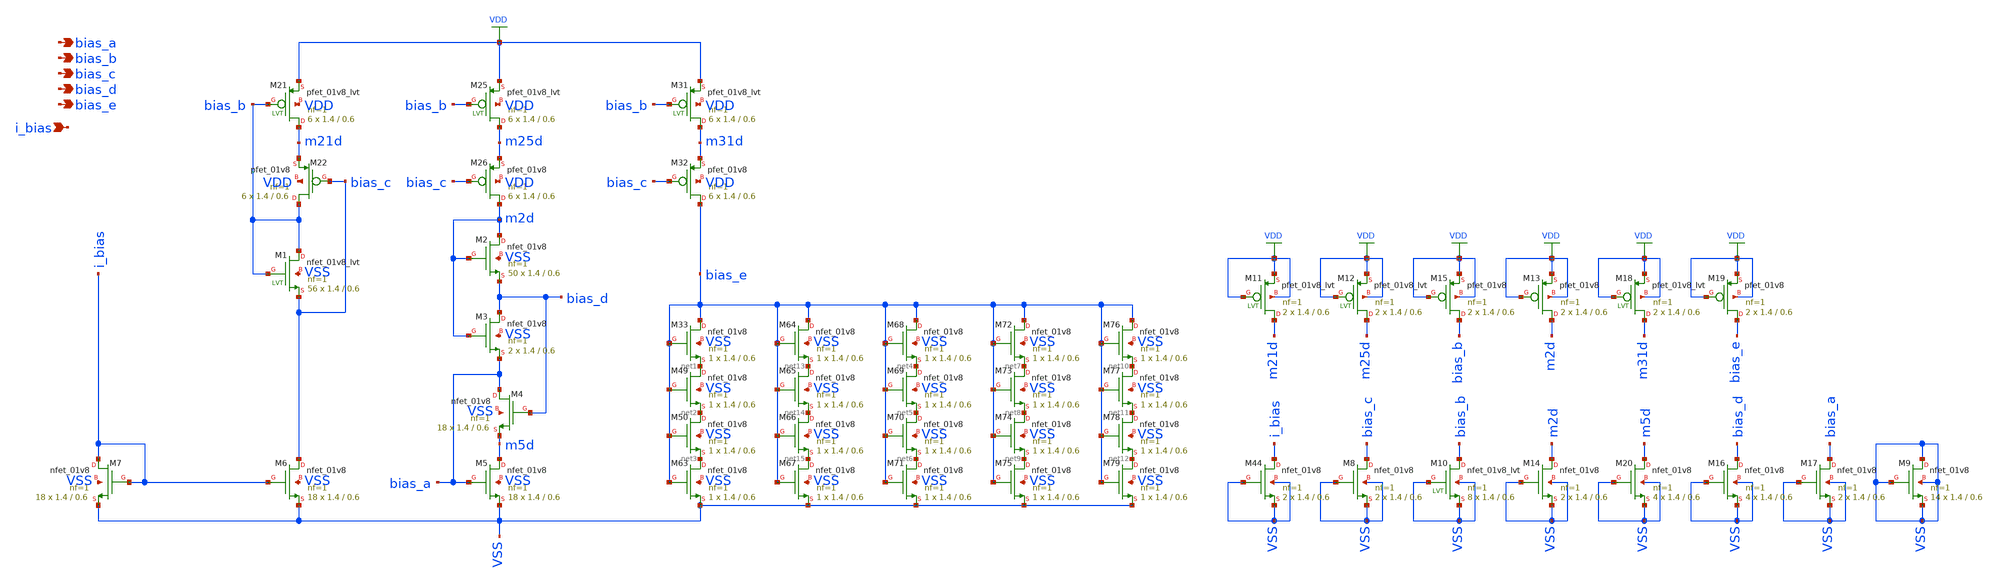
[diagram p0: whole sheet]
** sch_path: design/analog_modulator/schematic/folded_cascode_3_bias.sch
**.subckt folded_cascode_3_bias bias_a bias_b bias_c bias_d bias_e i_bias
*.opin bias_a
*.opin bias_b
*.opin bias_c
*.opin bias_d
*.opin bias_e
*.ipin i_bias
XM22 bias_b bias_c m21d VDD sky130_fd_pr__pfet_01v8 L=0.6 W=1.4 nf=1 ad='int((nf+1)/2) * W/nf * 0.29'
+ as='int((nf+2)/2) * W/nf * 0.29' pd='2*int((nf+1)/2) * (W/nf + 0.29)' ps='2*int((nf+2)/2) * (W/nf + 0.29)'
+ nrd='0.29 / W' nrs='0.29 / W' sa=0 sb=0 sd=0 mult=6 m=6
XM26 m2d bias_c m25d VDD sky130_fd_pr__pfet_01v8 L=0.6 W=1.4 nf=1 ad='int((nf+1)/2) * W/nf * 0.29' as='int((nf+2)/2) * W/nf * 0.29'
+ pd='2*int((nf+1)/2) * (W/nf + 0.29)' ps='2*int((nf+2)/2) * (W/nf + 0.29)' nrd='0.29 / W' nrs='0.29 / W'
+ sa=0 sb=0 sd=0 mult=6 m=6
XM32 bias_e bias_c m31d VDD sky130_fd_pr__pfet_01v8 L=0.6 W=1.4 nf=1 ad='int((nf+1)/2) * W/nf * 0.29'
+ as='int((nf+2)/2) * W/nf * 0.29' pd='2*int((nf+1)/2) * (W/nf + 0.29)' ps='2*int((nf+2)/2) * (W/nf + 0.29)'
+ nrd='0.29 / W' nrs='0.29 / W' sa=0 sb=0 sd=0 mult=6 m=6
XM21 m21d bias_b VDD VDD sky130_fd_pr__pfet_01v8_lvt L=0.6 W=1.4 nf=1 ad='int((nf+1)/2) * W/nf * 0.29'
+ as='int((nf+2)/2) * W/nf * 0.29' pd='2*int((nf+1)/2) * (W/nf + 0.29)' ps='2*int((nf+2)/2) * (W/nf + 0.29)'
+ nrd='0.29 / W' nrs='0.29 / W' sa=0 sb=0 sd=0 mult=6 m=6
XM25 m25d bias_b VDD VDD sky130_fd_pr__pfet_01v8_lvt L=0.6 W=1.4 nf=1 ad='int((nf+1)/2) * W/nf * 0.29'
+ as='int((nf+2)/2) * W/nf * 0.29' pd='2*int((nf+1)/2) * (W/nf + 0.29)' ps='2*int((nf+2)/2) * (W/nf + 0.29)'
+ nrd='0.29 / W' nrs='0.29 / W' sa=0 sb=0 sd=0 mult=6 m=6
XM31 m31d bias_b VDD VDD sky130_fd_pr__pfet_01v8_lvt L=0.6 W=1.4 nf=1 ad='int((nf+1)/2) * W/nf * 0.29'
+ as='int((nf+2)/2) * W/nf * 0.29' pd='2*int((nf+1)/2) * (W/nf + 0.29)' ps='2*int((nf+2)/2) * (W/nf + 0.29)'
+ nrd='0.29 / W' nrs='0.29 / W' sa=0 sb=0 sd=0 mult=6 m=6
XM1 bias_b bias_b bias_c VSS sky130_fd_pr__nfet_01v8_lvt L=0.6 W=1.4 nf=1 ad='int((nf+1)/2) * W/nf * 0.29'
+ as='int((nf+2)/2) * W/nf * 0.29' pd='2*int((nf+1)/2) * (W/nf + 0.29)' ps='2*int((nf+2)/2) * (W/nf + 0.29)'
+ nrd='0.29 / W' nrs='0.29 / W' sa=0 sb=0 sd=0 mult=56 m=56
XM2 m2d m2d bias_d VSS sky130_fd_pr__nfet_01v8 L=0.6 W=1.4 nf=1 ad='int((nf+1)/2) * W/nf * 0.29' as='int((nf+2)/2) * W/nf * 0.29'
+ pd='2*int((nf+1)/2) * (W/nf + 0.29)' ps='2*int((nf+2)/2) * (W/nf + 0.29)' nrd='0.29 / W' nrs='0.29 / W'
+ sa=0 sb=0 sd=0 mult=50 m=50
XM3 bias_d m2d bias_a VSS sky130_fd_pr__nfet_01v8 L=0.6 W=1.4 nf=1 ad='int((nf+1)/2) * W/nf * 0.29' as='int((nf+2)/2) * W/nf * 0.29'
+ pd='2*int((nf+1)/2) * (W/nf + 0.29)' ps='2*int((nf+2)/2) * (W/nf + 0.29)' nrd='0.29 / W' nrs='0.29 / W'
+ sa=0 sb=0 sd=0 mult=2 m=2
XM4 bias_a bias_d m5d VSS sky130_fd_pr__nfet_01v8 L=0.6 W=1.4 nf=1 ad='int((nf+1)/2) * W/nf * 0.29' as='int((nf+2)/2) * W/nf * 0.29'
+ pd='2*int((nf+1)/2) * (W/nf + 0.29)' ps='2*int((nf+2)/2) * (W/nf + 0.29)' nrd='0.29 / W' nrs='0.29 / W'
+ sa=0 sb=0 sd=0 mult=18 m=18
XM5 m5d bias_a VSS VSS sky130_fd_pr__nfet_01v8 L=0.6 W=1.4 nf=1 ad='int((nf+1)/2) * W/nf * 0.29' as='int((nf+2)/2) * W/nf * 0.29'
+ pd='2*int((nf+1)/2) * (W/nf + 0.29)' ps='2*int((nf+2)/2) * (W/nf + 0.29)' nrd='0.29 / W' nrs='0.29 / W'
+ sa=0 sb=0 sd=0 mult=18 m=18
XM6 bias_c i_bias VSS VSS sky130_fd_pr__nfet_01v8 L=0.6 W=1.4 nf=1 ad='int((nf+1)/2) * W/nf * 0.29' as='int((nf+2)/2) * W/nf * 0.29'
+ pd='2*int((nf+1)/2) * (W/nf + 0.29)' ps='2*int((nf+2)/2) * (W/nf + 0.29)' nrd='0.29 / W' nrs='0.29 / W'
+ sa=0 sb=0 sd=0 mult=18 m=18
XM7 i_bias i_bias VSS VSS sky130_fd_pr__nfet_01v8 L=0.6 W=1.4 nf=1 ad='int((nf+1)/2) * W/nf * 0.29' as='int((nf+2)/2) * W/nf * 0.29'
+ pd='2*int((nf+1)/2) * (W/nf + 0.29)' ps='2*int((nf+2)/2) * (W/nf + 0.29)' nrd='0.29 / W' nrs='0.29 / W'
+ sa=0 sb=0 sd=0 mult=18 m=18
XM33 bias_e bias_e net1 VSS sky130_fd_pr__nfet_01v8 L=0.6 W=1.4 nf=1 ad='int((nf+1)/2) * W/nf * 0.29'
+ as='int((nf+2)/2) * W/nf * 0.29' pd='2*int((nf+1)/2) * (W/nf + 0.29)' ps='2*int((nf+2)/2) * (W/nf + 0.29)'
+ nrd='0.29 / W' nrs='0.29 / W' sa=0 sb=0 sd=0 mult=1 m=1
XM49 net1 bias_e net2 VSS sky130_fd_pr__nfet_01v8 L=0.6 W=1.4 nf=1 ad='int((nf+1)/2) * W/nf * 0.29' as='int((nf+2)/2) * W/nf * 0.29'
+ pd='2*int((nf+1)/2) * (W/nf + 0.29)' ps='2*int((nf+2)/2) * (W/nf + 0.29)' nrd='0.29 / W' nrs='0.29 / W'
+ sa=0 sb=0 sd=0 mult=1 m=1
XM50 net2 bias_e net3 VSS sky130_fd_pr__nfet_01v8 L=0.6 W=1.4 nf=1 ad='int((nf+1)/2) * W/nf * 0.29' as='int((nf+2)/2) * W/nf * 0.29'
+ pd='2*int((nf+1)/2) * (W/nf + 0.29)' ps='2*int((nf+2)/2) * (W/nf + 0.29)' nrd='0.29 / W' nrs='0.29 / W'
+ sa=0 sb=0 sd=0 mult=1 m=1
XM63 net3 bias_e VSS VSS sky130_fd_pr__nfet_01v8 L=0.6 W=1.4 nf=1 ad='int((nf+1)/2) * W/nf * 0.29' as='int((nf+2)/2) * W/nf * 0.29'
+ pd='2*int((nf+1)/2) * (W/nf + 0.29)' ps='2*int((nf+2)/2) * (W/nf + 0.29)' nrd='0.29 / W' nrs='0.29 / W'
+ sa=0 sb=0 sd=0 mult=1 m=1
XM68 bias_e bias_e net4 VSS sky130_fd_pr__nfet_01v8 L=0.6 W=1.4 nf=1 ad='int((nf+1)/2) * W/nf * 0.29'
+ as='int((nf+2)/2) * W/nf * 0.29' pd='2*int((nf+1)/2) * (W/nf + 0.29)' ps='2*int((nf+2)/2) * (W/nf + 0.29)'
+ nrd='0.29 / W' nrs='0.29 / W' sa=0 sb=0 sd=0 mult=1 m=1
XM69 net4 bias_e net5 VSS sky130_fd_pr__nfet_01v8 L=0.6 W=1.4 nf=1 ad='int((nf+1)/2) * W/nf * 0.29' as='int((nf+2)/2) * W/nf * 0.29'
+ pd='2*int((nf+1)/2) * (W/nf + 0.29)' ps='2*int((nf+2)/2) * (W/nf + 0.29)' nrd='0.29 / W' nrs='0.29 / W'
+ sa=0 sb=0 sd=0 mult=1 m=1
XM70 net5 bias_e net6 VSS sky130_fd_pr__nfet_01v8 L=0.6 W=1.4 nf=1 ad='int((nf+1)/2) * W/nf * 0.29' as='int((nf+2)/2) * W/nf * 0.29'
+ pd='2*int((nf+1)/2) * (W/nf + 0.29)' ps='2*int((nf+2)/2) * (W/nf + 0.29)' nrd='0.29 / W' nrs='0.29 / W'
+ sa=0 sb=0 sd=0 mult=1 m=1
XM71 net6 bias_e VSS VSS sky130_fd_pr__nfet_01v8 L=0.6 W=1.4 nf=1 ad='int((nf+1)/2) * W/nf * 0.29' as='int((nf+2)/2) * W/nf * 0.29'
+ pd='2*int((nf+1)/2) * (W/nf + 0.29)' ps='2*int((nf+2)/2) * (W/nf + 0.29)' nrd='0.29 / W' nrs='0.29 / W'
+ sa=0 sb=0 sd=0 mult=1 m=1
XM72 bias_e bias_e net7 VSS sky130_fd_pr__nfet_01v8 L=0.6 W=1.4 nf=1 ad='int((nf+1)/2) * W/nf * 0.29'
+ as='int((nf+2)/2) * W/nf * 0.29' pd='2*int((nf+1)/2) * (W/nf + 0.29)' ps='2*int((nf+2)/2) * (W/nf + 0.29)'
+ nrd='0.29 / W' nrs='0.29 / W' sa=0 sb=0 sd=0 mult=1 m=1
XM73 net7 bias_e net8 VSS sky130_fd_pr__nfet_01v8 L=0.6 W=1.4 nf=1 ad='int((nf+1)/2) * W/nf * 0.29' as='int((nf+2)/2) * W/nf * 0.29'
+ pd='2*int((nf+1)/2) * (W/nf + 0.29)' ps='2*int((nf+2)/2) * (W/nf + 0.29)' nrd='0.29 / W' nrs='0.29 / W'
+ sa=0 sb=0 sd=0 mult=1 m=1
XM74 net8 bias_e net9 VSS sky130_fd_pr__nfet_01v8 L=0.6 W=1.4 nf=1 ad='int((nf+1)/2) * W/nf * 0.29' as='int((nf+2)/2) * W/nf * 0.29'
+ pd='2*int((nf+1)/2) * (W/nf + 0.29)' ps='2*int((nf+2)/2) * (W/nf + 0.29)' nrd='0.29 / W' nrs='0.29 / W'
+ sa=0 sb=0 sd=0 mult=1 m=1
XM75 net9 bias_e VSS VSS sky130_fd_pr__nfet_01v8 L=0.6 W=1.4 nf=1 ad='int((nf+1)/2) * W/nf * 0.29' as='int((nf+2)/2) * W/nf * 0.29'
+ pd='2*int((nf+1)/2) * (W/nf + 0.29)' ps='2*int((nf+2)/2) * (W/nf + 0.29)' nrd='0.29 / W' nrs='0.29 / W'
+ sa=0 sb=0 sd=0 mult=1 m=1
XM76 bias_e bias_e net10 VSS sky130_fd_pr__nfet_01v8 L=0.6 W=1.4 nf=1 ad='int((nf+1)/2) * W/nf * 0.29'
+ as='int((nf+2)/2) * W/nf * 0.29' pd='2*int((nf+1)/2) * (W/nf + 0.29)' ps='2*int((nf+2)/2) * (W/nf + 0.29)'
+ nrd='0.29 / W' nrs='0.29 / W' sa=0 sb=0 sd=0 mult=1 m=1
XM77 net10 bias_e net11 VSS sky130_fd_pr__nfet_01v8 L=0.6 W=1.4 nf=1 ad='int((nf+1)/2) * W/nf * 0.29'
+ as='int((nf+2)/2) * W/nf * 0.29' pd='2*int((nf+1)/2) * (W/nf + 0.29)' ps='2*int((nf+2)/2) * (W/nf + 0.29)'
+ nrd='0.29 / W' nrs='0.29 / W' sa=0 sb=0 sd=0 mult=1 m=1
XM78 net11 bias_e net12 VSS sky130_fd_pr__nfet_01v8 L=0.6 W=1.4 nf=1 ad='int((nf+1)/2) * W/nf * 0.29'
+ as='int((nf+2)/2) * W/nf * 0.29' pd='2*int((nf+1)/2) * (W/nf + 0.29)' ps='2*int((nf+2)/2) * (W/nf + 0.29)'
+ nrd='0.29 / W' nrs='0.29 / W' sa=0 sb=0 sd=0 mult=1 m=1
XM79 net12 bias_e VSS VSS sky130_fd_pr__nfet_01v8 L=0.6 W=1.4 nf=1 ad='int((nf+1)/2) * W/nf * 0.29' as='int((nf+2)/2) * W/nf * 0.29'
+ pd='2*int((nf+1)/2) * (W/nf + 0.29)' ps='2*int((nf+2)/2) * (W/nf + 0.29)' nrd='0.29 / W' nrs='0.29 / W'
+ sa=0 sb=0 sd=0 mult=1 m=1
XM64 bias_e bias_e net13 VSS sky130_fd_pr__nfet_01v8 L=0.6 W=1.4 nf=1 ad='int((nf+1)/2) * W/nf * 0.29'
+ as='int((nf+2)/2) * W/nf * 0.29' pd='2*int((nf+1)/2) * (W/nf + 0.29)' ps='2*int((nf+2)/2) * (W/nf + 0.29)'
+ nrd='0.29 / W' nrs='0.29 / W' sa=0 sb=0 sd=0 mult=1 m=1
XM65 net13 bias_e net14 VSS sky130_fd_pr__nfet_01v8 L=0.6 W=1.4 nf=1 ad='int((nf+1)/2) * W/nf * 0.29'
+ as='int((nf+2)/2) * W/nf * 0.29' pd='2*int((nf+1)/2) * (W/nf + 0.29)' ps='2*int((nf+2)/2) * (W/nf + 0.29)'
+ nrd='0.29 / W' nrs='0.29 / W' sa=0 sb=0 sd=0 mult=1 m=1
XM66 net14 bias_e net15 VSS sky130_fd_pr__nfet_01v8 L=0.6 W=1.4 nf=1 ad='int((nf+1)/2) * W/nf * 0.29'
+ as='int((nf+2)/2) * W/nf * 0.29' pd='2*int((nf+1)/2) * (W/nf + 0.29)' ps='2*int((nf+2)/2) * (W/nf + 0.29)'
+ nrd='0.29 / W' nrs='0.29 / W' sa=0 sb=0 sd=0 mult=1 m=1
XM67 net15 bias_e VSS VSS sky130_fd_pr__nfet_01v8 L=0.6 W=1.4 nf=1 ad='int((nf+1)/2) * W/nf * 0.29' as='int((nf+2)/2) * W/nf * 0.29'
+ pd='2*int((nf+1)/2) * (W/nf + 0.29)' ps='2*int((nf+2)/2) * (W/nf + 0.29)' nrd='0.29 / W' nrs='0.29 / W'
+ sa=0 sb=0 sd=0 mult=1 m=1
XM44 i_bias VSS VSS VSS sky130_fd_pr__nfet_01v8 L=0.6 W=1.4 nf=1 ad='int((nf+1)/2) * W/nf * 0.29' as='int((nf+2)/2) * W/nf * 0.29'
+ pd='2*int((nf+1)/2) * (W/nf + 0.29)' ps='2*int((nf+2)/2) * (W/nf + 0.29)' nrd='0.29 / W' nrs='0.29 / W'
+ sa=0 sb=0 sd=0 mult=2 m=2
XM8 bias_c VSS VSS VSS sky130_fd_pr__nfet_01v8 L=0.6 W=1.4 nf=1 ad='int((nf+1)/2) * W/nf * 0.29' as='int((nf+2)/2) * W/nf * 0.29'
+ pd='2*int((nf+1)/2) * (W/nf + 0.29)' ps='2*int((nf+2)/2) * (W/nf + 0.29)' nrd='0.29 / W' nrs='0.29 / W'
+ sa=0 sb=0 sd=0 mult=2 m=2
XM9 VSS VSS VSS VSS sky130_fd_pr__nfet_01v8 L=0.6 W=1.4 nf=1 ad='int((nf+1)/2) * W/nf * 0.29' as='int((nf+2)/2) * W/nf * 0.29'
+ pd='2*int((nf+1)/2) * (W/nf + 0.29)' ps='2*int((nf+2)/2) * (W/nf + 0.29)' nrd='0.29 / W' nrs='0.29 / W'
+ sa=0 sb=0 sd=0 mult=14 m=14
XM11 m21d VDD VDD VDD sky130_fd_pr__pfet_01v8_lvt L=0.6 W=1.4 nf=1 ad='int((nf+1)/2) * W/nf * 0.29' as='int((nf+2)/2) * W/nf * 0.29'
+ pd='2*int((nf+1)/2) * (W/nf + 0.29)' ps='2*int((nf+2)/2) * (W/nf + 0.29)' nrd='0.29 / W' nrs='0.29 / W'
+ sa=0 sb=0 sd=0 mult=2 m=2
XM12 m25d VDD VDD VDD sky130_fd_pr__pfet_01v8_lvt L=0.6 W=1.4 nf=1 ad='int((nf+1)/2) * W/nf * 0.29' as='int((nf+2)/2) * W/nf * 0.29'
+ pd='2*int((nf+1)/2) * (W/nf + 0.29)' ps='2*int((nf+2)/2) * (W/nf + 0.29)' nrd='0.29 / W' nrs='0.29 / W'
+ sa=0 sb=0 sd=0 mult=2 m=2
XM13 m2d VDD VDD VDD sky130_fd_pr__pfet_01v8 L=0.6 W=1.4 nf=1 ad='int((nf+1)/2) * W/nf * 0.29' as='int((nf+2)/2) * W/nf * 0.29'
+ pd='2*int((nf+1)/2) * (W/nf + 0.29)' ps='2*int((nf+2)/2) * (W/nf + 0.29)' nrd='0.29 / W' nrs='0.29 / W'
+ sa=0 sb=0 sd=0 mult=2 m=2
XM14 m2d VSS VSS VSS sky130_fd_pr__nfet_01v8 L=0.6 W=1.4 nf=1 ad='int((nf+1)/2) * W/nf * 0.29' as='int((nf+2)/2) * W/nf * 0.29'
+ pd='2*int((nf+1)/2) * (W/nf + 0.29)' ps='2*int((nf+2)/2) * (W/nf + 0.29)' nrd='0.29 / W' nrs='0.29 / W'
+ sa=0 sb=0 sd=0 mult=2 m=2
XM10 bias_b VSS VSS VSS sky130_fd_pr__nfet_01v8_lvt L=0.6 W=1.4 nf=1 ad='int((nf+1)/2) * W/nf * 0.29'
+ as='int((nf+2)/2) * W/nf * 0.29' pd='2*int((nf+1)/2) * (W/nf + 0.29)' ps='2*int((nf+2)/2) * (W/nf + 0.29)'
+ nrd='0.29 / W' nrs='0.29 / W' sa=0 sb=0 sd=0 mult=8 m=8
XM15 bias_b VDD VDD VDD sky130_fd_pr__pfet_01v8 L=0.6 W=1.4 nf=1 ad='int((nf+1)/2) * W/nf * 0.29' as='int((nf+2)/2) * W/nf * 0.29'
+ pd='2*int((nf+1)/2) * (W/nf + 0.29)' ps='2*int((nf+2)/2) * (W/nf + 0.29)' nrd='0.29 / W' nrs='0.29 / W'
+ sa=0 sb=0 sd=0 mult=2 m=2
XM16 bias_d VSS VSS VSS sky130_fd_pr__nfet_01v8 L=0.6 W=1.4 nf=1 ad='int((nf+1)/2) * W/nf * 0.29' as='int((nf+2)/2) * W/nf * 0.29'
+ pd='2*int((nf+1)/2) * (W/nf + 0.29)' ps='2*int((nf+2)/2) * (W/nf + 0.29)' nrd='0.29 / W' nrs='0.29 / W'
+ sa=0 sb=0 sd=0 mult=4 m=4
XM17 bias_a VSS VSS VSS sky130_fd_pr__nfet_01v8 L=0.6 W=1.4 nf=1 ad='int((nf+1)/2) * W/nf * 0.29' as='int((nf+2)/2) * W/nf * 0.29'
+ pd='2*int((nf+1)/2) * (W/nf + 0.29)' ps='2*int((nf+2)/2) * (W/nf + 0.29)' nrd='0.29 / W' nrs='0.29 / W'
+ sa=0 sb=0 sd=0 mult=2 m=2
XM18 m31d VDD VDD VDD sky130_fd_pr__pfet_01v8_lvt L=0.6 W=1.4 nf=1 ad='int((nf+1)/2) * W/nf * 0.29' as='int((nf+2)/2) * W/nf * 0.29'
+ pd='2*int((nf+1)/2) * (W/nf + 0.29)' ps='2*int((nf+2)/2) * (W/nf + 0.29)' nrd='0.29 / W' nrs='0.29 / W'
+ sa=0 sb=0 sd=0 mult=2 m=2
XM19 bias_e VDD VDD VDD sky130_fd_pr__pfet_01v8 L=0.6 W=1.4 nf=1 ad='int((nf+1)/2) * W/nf * 0.29' as='int((nf+2)/2) * W/nf * 0.29'
+ pd='2*int((nf+1)/2) * (W/nf + 0.29)' ps='2*int((nf+2)/2) * (W/nf + 0.29)' nrd='0.29 / W' nrs='0.29 / W'
+ sa=0 sb=0 sd=0 mult=2 m=2
XM20 m5d VSS VSS VSS sky130_fd_pr__nfet_01v8 L=0.6 W=1.4 nf=1 ad='int((nf+1)/2) * W/nf * 0.29' as='int((nf+2)/2) * W/nf * 0.29'
+ pd='2*int((nf+1)/2) * (W/nf + 0.29)' ps='2*int((nf+2)/2) * (W/nf + 0.29)' nrd='0.29 / W' nrs='0.29 / W'
+ sa=0 sb=0 sd=0 mult=4 m=4
**.ends
.GLOBAL VDD
.end
